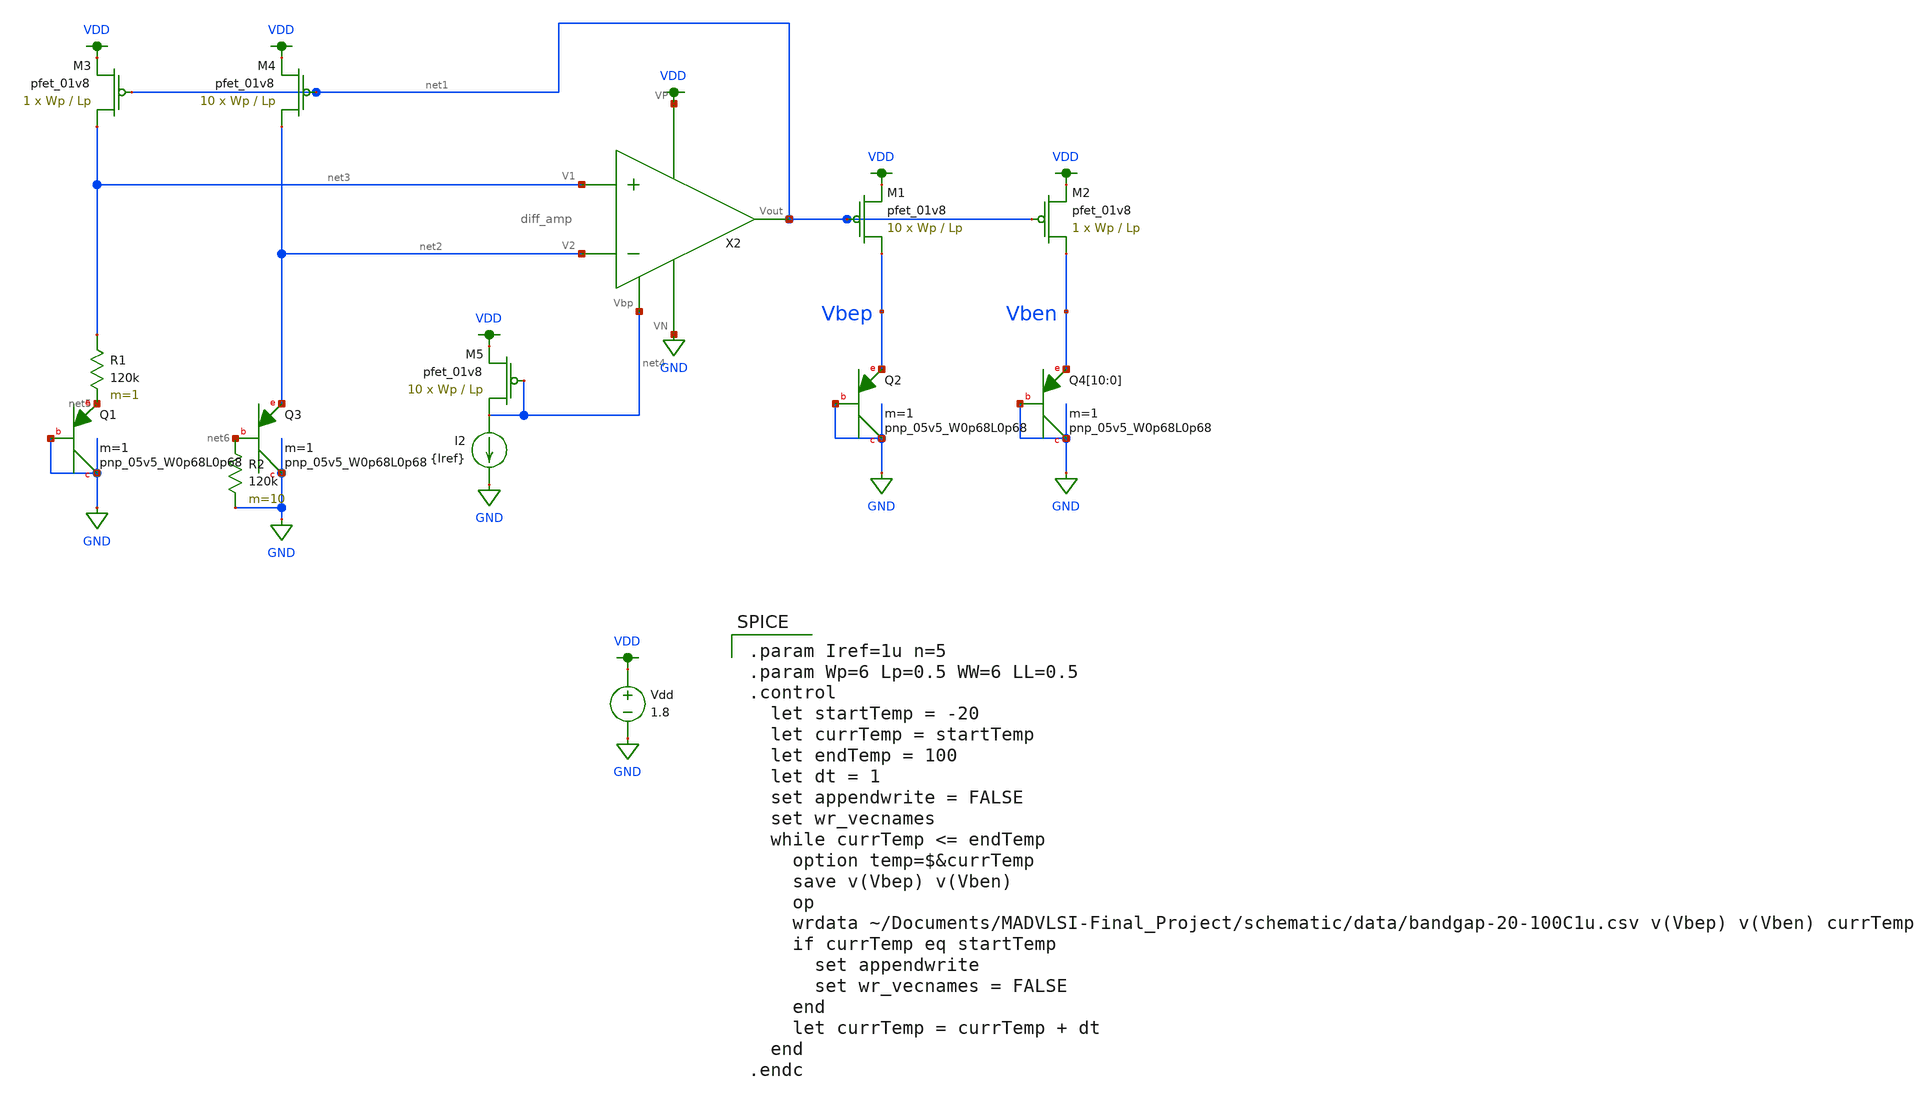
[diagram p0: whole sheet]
** sch_path: schematic/test/archive/bandgap_test.sch
**.subckt bandgap_test
XQ2 GND GND Vbep sky130_fd_pr__pnp_05v5_W0p68L0p68 m=1
Vdd VDD GND 1.8
XM1 Vbep net1 VDD VDD sky130_fd_pr__pfet_01v8 L=Lp W=Wp nf=1 ad='int((nf+1)/2) * W/nf * 0.29' as='int((nf+2)/2) * W/nf * 0.29'
+ pd='2*int((nf+1)/2) * (W/nf + 0.29)' ps='2*int((nf+2)/2) * (W/nf + 0.29)' nrd='0.29 / W' nrs='0.29 / W'
+ sa=0 sb=0 sd=0 mult=10 m=10
XM2 Vben net1 VDD VDD sky130_fd_pr__pfet_01v8 L=Lp W=Wp nf=1 ad='int((nf+1)/2) * W/nf * 0.29' as='int((nf+2)/2) * W/nf * 0.29'
+ pd='2*int((nf+1)/2) * (W/nf + 0.29)' ps='2*int((nf+2)/2) * (W/nf + 0.29)' nrd='0.29 / W' nrs='0.29 / W'
+ sa=0 sb=0 sd=0 mult=1 m=1
XQ4[10] GND GND Vben sky130_fd_pr__pnp_05v5_W0p68L0p68 m=1
XQ4[9] GND GND Vben sky130_fd_pr__pnp_05v5_W0p68L0p68 m=1
XQ4[8] GND GND Vben sky130_fd_pr__pnp_05v5_W0p68L0p68 m=1
XQ4[7] GND GND Vben sky130_fd_pr__pnp_05v5_W0p68L0p68 m=1
XQ4[6] GND GND Vben sky130_fd_pr__pnp_05v5_W0p68L0p68 m=1
XQ4[5] GND GND Vben sky130_fd_pr__pnp_05v5_W0p68L0p68 m=1
XQ4[4] GND GND Vben sky130_fd_pr__pnp_05v5_W0p68L0p68 m=1
XQ4[3] GND GND Vben sky130_fd_pr__pnp_05v5_W0p68L0p68 m=1
XQ4[2] GND GND Vben sky130_fd_pr__pnp_05v5_W0p68L0p68 m=1
XQ4[1] GND GND Vben sky130_fd_pr__pnp_05v5_W0p68L0p68 m=1
XQ4[0] GND GND Vben sky130_fd_pr__pnp_05v5_W0p68L0p68 m=1
X2 VDD net4 net1 net3 net2 GND diff_amp
XQ1 GND GND net5 sky130_fd_pr__pnp_05v5_W0p68L0p68 m=1
XQ3 GND net6 net2 sky130_fd_pr__pnp_05v5_W0p68L0p68 m=1
R1 net3 net5 120k m=1
R2 net6 GND 120k m=10
XM3 net3 net1 VDD VDD sky130_fd_pr__pfet_01v8 L=Lp W=Wp nf=1 ad='int((nf+1)/2) * W/nf * 0.29' as='int((nf+2)/2) * W/nf * 0.29'
+ pd='2*int((nf+1)/2) * (W/nf + 0.29)' ps='2*int((nf+2)/2) * (W/nf + 0.29)' nrd='0.29 / W' nrs='0.29 / W'
+ sa=0 sb=0 sd=0 mult=1 m=1
XM4 net2 net1 VDD VDD sky130_fd_pr__pfet_01v8 L=Lp W=Wp nf=1 ad='int((nf+1)/2) * W/nf * 0.29' as='int((nf+2)/2) * W/nf * 0.29'
+ pd='2*int((nf+1)/2) * (W/nf + 0.29)' ps='2*int((nf+2)/2) * (W/nf + 0.29)' nrd='0.29 / W' nrs='0.29 / W'
+ sa=0 sb=0 sd=0 mult=10 m=10
I2 net4 GND {Iref}
XM5 net4 net4 VDD VDD sky130_fd_pr__pfet_01v8 L=Lp W=Wp nf=1 ad='int((nf+1)/2) * W/nf * 0.29' as='int((nf+2)/2) * W/nf * 0.29'
+ pd='2*int((nf+1)/2) * (W/nf + 0.29)' ps='2*int((nf+2)/2) * (W/nf + 0.29)' nrd='0.29 / W' nrs='0.29 / W'
+ sa=0 sb=0 sd=0 mult=10 m=10
**** begin user architecture code

.option wnflag=1
.param MC_SWITCH=0.0
.lib ~/skywater/skywater-pdk/libraries/sky130_fd_pr_ngspice/latest/models/sky130.lib.spice tt


.param Iref=1u n=5
.param Wp=6 Lp=0.5 WW=6 LL=0.5
.control
  let startTemp = -20
  let currTemp = startTemp
  let endTemp = 100
  let dt = 1
  set appendwrite = FALSE
  set wr_vecnames
  while currTemp <= endTemp
    option temp=$&currTemp
    save v(Vbep) v(Vben)
    op
    wrdata ~/Documents/MADVLSI-Final_Project/schematic/data/bandgap-20-100C1u.csv v(Vbep) v(Vben)
+ currTemp
    if currTemp eq startTemp
      set appendwrite
      set wr_vecnames = FALSE
    end
    let currTemp = currTemp + dt
  end
.endc

**** end user architecture code
**.ends
.GLOBAL GND
.GLOBAL VDD
.end
